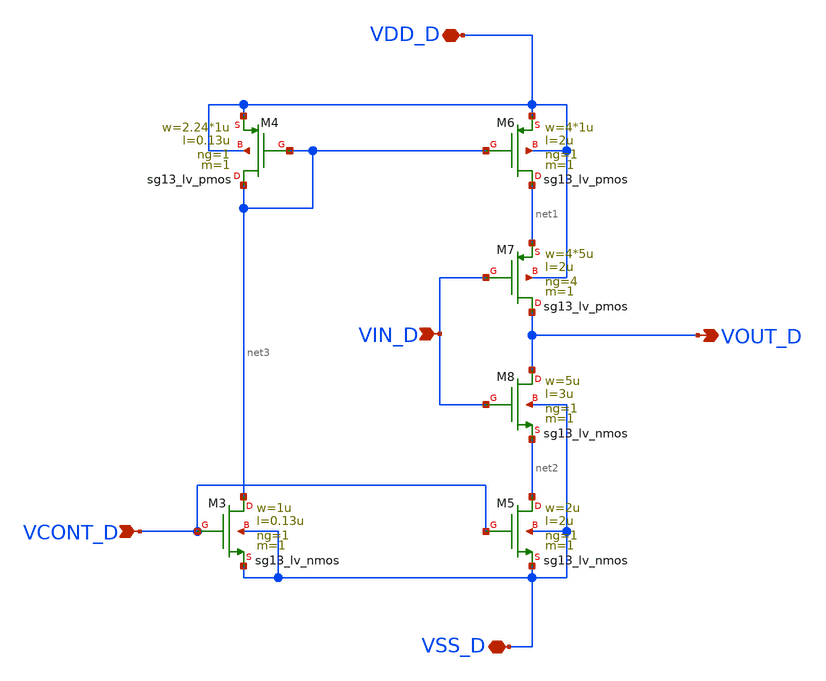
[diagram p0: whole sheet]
** sch_path: sch/delay_variable/delay_variable.sch
**.subckt delay_variable VDD_D VOUT_D VCONT_D VIN_D VSS_D
*.iopin VDD_D
*.opin VOUT_D
*.ipin VCONT_D
*.ipin VIN_D
*.iopin VSS_D
XM3 net3 VCONT_D VSS_D VSS_D sg13_lv_nmos w=1u l=0.13u ng=1 m=1 mm_ok=1
XM5 net2 VCONT_D VSS_D VSS_D sg13_lv_nmos w=2u l=2u ng=1 m=1 mm_ok=1
XM4 net3 net3 VDD_D VDD_D sg13_lv_pmos w=2.24*1u l=0.13u ng=1 m=1 mm_ok=1
XM6 net1 net3 VDD_D VDD_D sg13_lv_pmos w=4*1u l=2u ng=1 m=1 mm_ok=1
XM7 VOUT_D VIN_D net1 VDD_D sg13_lv_pmos w=4*5u l=2u ng=4 m=1 mm_ok=1
XM8 VOUT_D VIN_D net2 VSS_D sg13_lv_nmos w=5u l=3u ng=1 m=1 mm_ok=1
**.ends
.end
